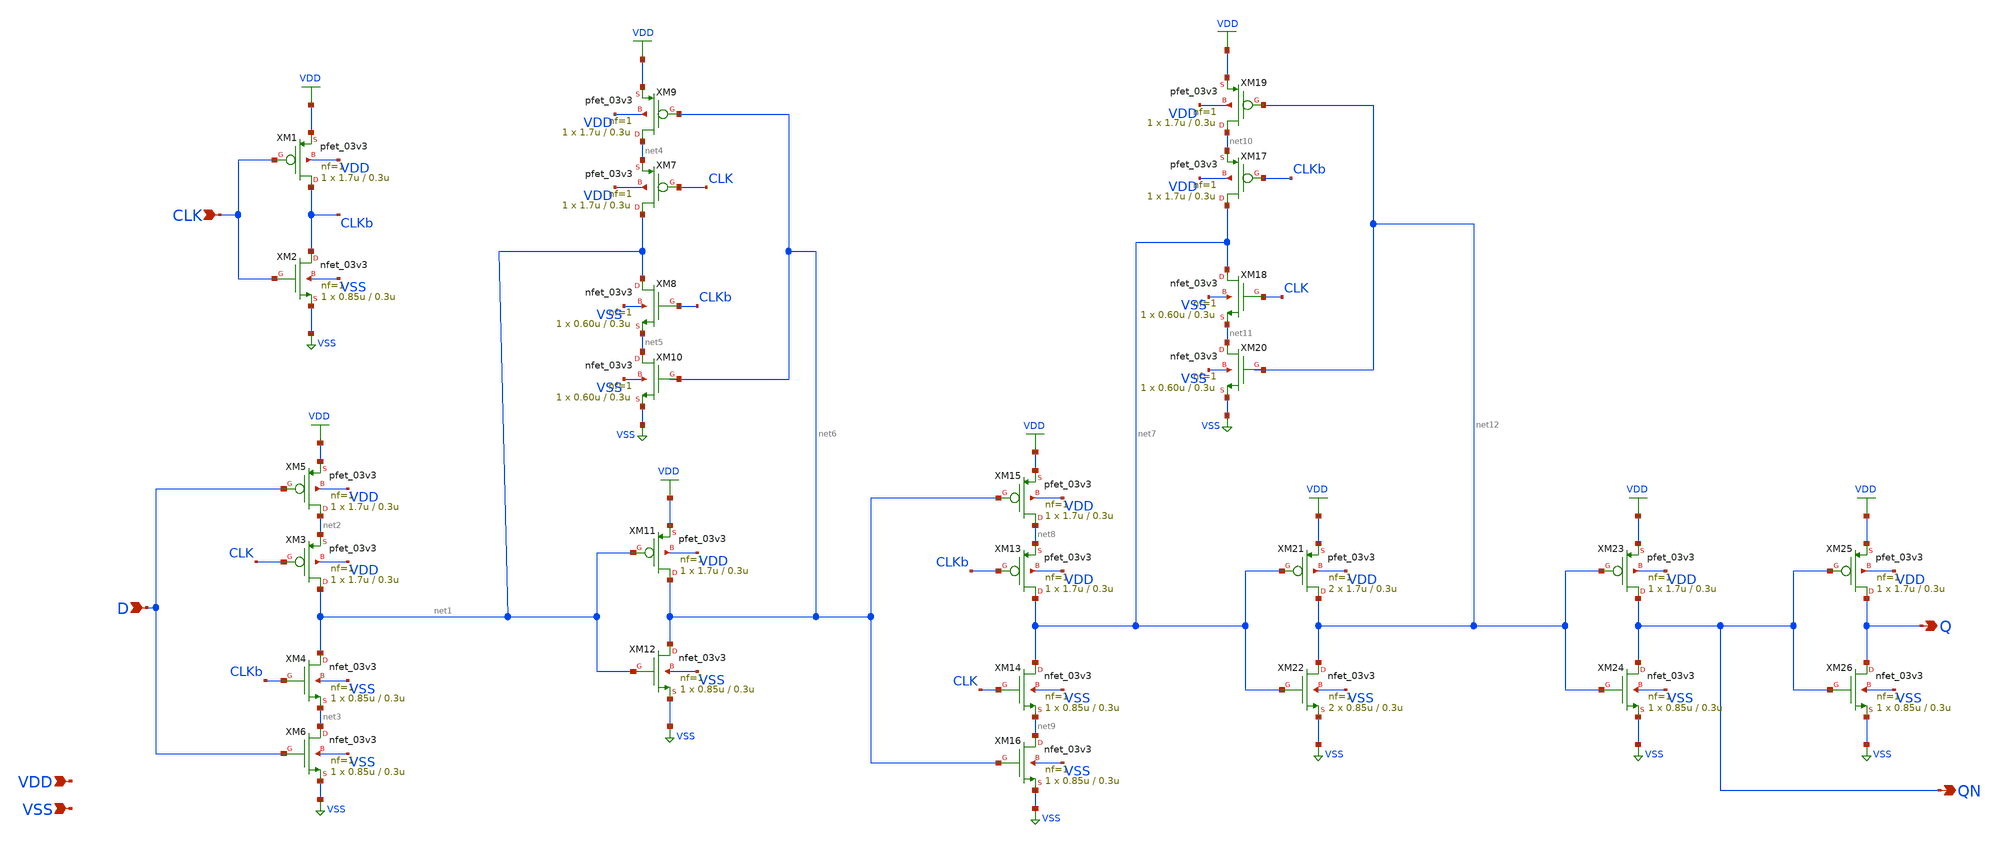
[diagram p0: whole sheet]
** sch_path: gf180mcu_osu_sc_gp9t3v3/xschem/gf180mcu_osu_sc_gp9t3v3__dff_1.sch
**.subckt gf180mcu_osu_sc_gp9t3v3__dff_1 D CLK Q QN VDD VSS
*.ipin D
*.ipin CLK
*.opin Q
*.opin QN
*.ipin VDD
*.ipin VSS
XM1 CLKb CLK VDD VDD pfet_03v3 L=0.3u W=1.7u nf=1 ad='int((nf+1)/2) * W/nf * 0.18u' as='int((nf+2)/2) * W/nf * 0.18u'
+ pd='2*int((nf+1)/2) * (W/nf + 0.18u)' ps='2*int((nf+2)/2) * (W/nf + 0.18u)' nrd='0.18u / W' nrs='0.18u / W'
+ sa=0 sb=0 sd=0 m=1
XM2 CLKb CLK VSS VSS nfet_03v3 L=0.3u W=0.85u nf=1 ad='int((nf+1)/2) * W/nf * 0.18u' as='int((nf+2)/2) * W/nf * 0.18u'
+ pd='2*int((nf+1)/2) * (W/nf + 0.18u)' ps='2*int((nf+2)/2) * (W/nf + 0.18u)' nrd='0.18u / W' nrs='0.18u / W'
+ sa=0 sb=0 sd=0 m=1
XM3 net1 CLK net2 VDD pfet_03v3 L=0.3u W=1.7u nf=1 ad='int((nf+1)/2) * W/nf * 0.18u' as='int((nf+2)/2) * W/nf * 0.18u'
+ pd='2*int((nf+1)/2) * (W/nf + 0.18u)' ps='2*int((nf+2)/2) * (W/nf + 0.18u)' nrd='0.18u / W' nrs='0.18u / W'
+ sa=0 sb=0 sd=0 m=1
XM4 net1 CLKb net3 VSS nfet_03v3 L=0.3u W=0.85u nf=1 ad='int((nf+1)/2) * W/nf * 0.18u' as='int((nf+2)/2) * W/nf * 0.18u'
+ pd='2*int((nf+1)/2) * (W/nf + 0.18u)' ps='2*int((nf+2)/2) * (W/nf + 0.18u)' nrd='0.18u / W' nrs='0.18u / W'
+ sa=0 sb=0 sd=0 m=1
XM5 net2 D VDD VDD pfet_03v3 L=0.3u W=1.7u nf=1 ad='int((nf+1)/2) * W/nf * 0.18u' as='int((nf+2)/2) * W/nf * 0.18u'
+ pd='2*int((nf+1)/2) * (W/nf + 0.18u)' ps='2*int((nf+2)/2) * (W/nf + 0.18u)' nrd='0.18u / W' nrs='0.18u / W'
+ sa=0 sb=0 sd=0 m=1
XM6 net3 D VSS VSS nfet_03v3 L=0.3u W=0.85u nf=1 ad='int((nf+1)/2) * W/nf * 0.18u' as='int((nf+2)/2) * W/nf * 0.18u'
+ pd='2*int((nf+1)/2) * (W/nf + 0.18u)' ps='2*int((nf+2)/2) * (W/nf + 0.18u)' nrd='0.18u / W' nrs='0.18u / W'
+ sa=0 sb=0 sd=0 m=1
XM7 net1 CLK net4 VDD pfet_03v3 L=0.3u W=1.7u nf=1 ad='int((nf+1)/2) * W/nf * 0.18u' as='int((nf+2)/2) * W/nf * 0.18u'
+ pd='2*int((nf+1)/2) * (W/nf + 0.18u)' ps='2*int((nf+2)/2) * (W/nf + 0.18u)' nrd='0.18u / W' nrs='0.18u / W'
+ sa=0 sb=0 sd=0 m=1
XM8 net1 CLKb net5 VSS nfet_03v3 L=0.3u W=0.60u nf=1 ad='int((nf+1)/2) * W/nf * 0.18u' as='int((nf+2)/2) * W/nf * 0.18u'
+ pd='2*int((nf+1)/2) * (W/nf + 0.18u)' ps='2*int((nf+2)/2) * (W/nf + 0.18u)' nrd='0.18u / W' nrs='0.18u / W'
+ sa=0 sb=0 sd=0 m=1
XM9 net4 net6 VDD VDD pfet_03v3 L=0.3u W=1.7u nf=1 ad='int((nf+1)/2) * W/nf * 0.18u' as='int((nf+2)/2) * W/nf * 0.18u'
+ pd='2*int((nf+1)/2) * (W/nf + 0.18u)' ps='2*int((nf+2)/2) * (W/nf + 0.18u)' nrd='0.18u / W' nrs='0.18u / W'
+ sa=0 sb=0 sd=0 m=1
XM10 net5 net6 VSS VSS nfet_03v3 L=0.3u W=0.60u nf=1 ad='int((nf+1)/2) * W/nf * 0.18u' as='int((nf+2)/2) * W/nf * 0.18u'
+ pd='2*int((nf+1)/2) * (W/nf + 0.18u)' ps='2*int((nf+2)/2) * (W/nf + 0.18u)' nrd='0.18u / W' nrs='0.18u / W'
+ sa=0 sb=0 sd=0 m=1
XM11 net6 net1 VDD VDD pfet_03v3 L=0.3u W=1.7u nf=1 ad='int((nf+1)/2) * W/nf * 0.18u' as='int((nf+2)/2) * W/nf * 0.18u'
+ pd='2*int((nf+1)/2) * (W/nf + 0.18u)' ps='2*int((nf+2)/2) * (W/nf + 0.18u)' nrd='0.18u / W' nrs='0.18u / W'
+ sa=0 sb=0 sd=0 m=1
XM12 net6 net1 VSS VSS nfet_03v3 L=0.3u W=0.85u nf=1 ad='int((nf+1)/2) * W/nf * 0.18u' as='int((nf+2)/2) * W/nf * 0.18u'
+ pd='2*int((nf+1)/2) * (W/nf + 0.18u)' ps='2*int((nf+2)/2) * (W/nf + 0.18u)' nrd='0.18u / W' nrs='0.18u / W'
+ sa=0 sb=0 sd=0 m=1
XM13 net7 CLKb net8 VDD pfet_03v3 L=0.3u W=1.7u nf=1 ad='int((nf+1)/2) * W/nf * 0.18u' as='int((nf+2)/2) * W/nf * 0.18u'
+ pd='2*int((nf+1)/2) * (W/nf + 0.18u)' ps='2*int((nf+2)/2) * (W/nf + 0.18u)' nrd='0.18u / W' nrs='0.18u / W'
+ sa=0 sb=0 sd=0 m=1
XM14 net7 CLK net9 VSS nfet_03v3 L=0.3u W=0.85u nf=1 ad='int((nf+1)/2) * W/nf * 0.18u' as='int((nf+2)/2) * W/nf * 0.18u'
+ pd='2*int((nf+1)/2) * (W/nf + 0.18u)' ps='2*int((nf+2)/2) * (W/nf + 0.18u)' nrd='0.18u / W' nrs='0.18u / W'
+ sa=0 sb=0 sd=0 m=1
XM15 net8 net6 VDD VDD pfet_03v3 L=0.3u W=1.7u nf=1 ad='int((nf+1)/2) * W/nf * 0.18u' as='int((nf+2)/2) * W/nf * 0.18u'
+ pd='2*int((nf+1)/2) * (W/nf + 0.18u)' ps='2*int((nf+2)/2) * (W/nf + 0.18u)' nrd='0.18u / W' nrs='0.18u / W'
+ sa=0 sb=0 sd=0 m=1
XM16 net9 net6 VSS VSS nfet_03v3 L=0.3u W=0.85u nf=1 ad='int((nf+1)/2) * W/nf * 0.18u' as='int((nf+2)/2) * W/nf * 0.18u'
+ pd='2*int((nf+1)/2) * (W/nf + 0.18u)' ps='2*int((nf+2)/2) * (W/nf + 0.18u)' nrd='0.18u / W' nrs='0.18u / W'
+ sa=0 sb=0 sd=0 m=1
XM17 net7 CLKb net10 VDD pfet_03v3 L=0.3u W=1.7u nf=1 ad='int((nf+1)/2) * W/nf * 0.18u' as='int((nf+2)/2) * W/nf * 0.18u'
+ pd='2*int((nf+1)/2) * (W/nf + 0.18u)' ps='2*int((nf+2)/2) * (W/nf + 0.18u)' nrd='0.18u / W' nrs='0.18u / W'
+ sa=0 sb=0 sd=0 m=1
XM18 net7 CLK net11 VSS nfet_03v3 L=0.3u W=0.60u nf=1 ad='int((nf+1)/2) * W/nf * 0.18u' as='int((nf+2)/2) * W/nf * 0.18u'
+ pd='2*int((nf+1)/2) * (W/nf + 0.18u)' ps='2*int((nf+2)/2) * (W/nf + 0.18u)' nrd='0.18u / W' nrs='0.18u / W'
+ sa=0 sb=0 sd=0 m=1
XM19 net10 net12 VDD VDD pfet_03v3 L=0.3u W=1.7u nf=1 ad='int((nf+1)/2) * W/nf * 0.18u' as='int((nf+2)/2) * W/nf * 0.18u'
+ pd='2*int((nf+1)/2) * (W/nf + 0.18u)' ps='2*int((nf+2)/2) * (W/nf + 0.18u)' nrd='0.18u / W' nrs='0.18u / W'
+ sa=0 sb=0 sd=0 m=1
XM20 net11 net12 VSS VSS nfet_03v3 L=0.3u W=0.60u nf=1 ad='int((nf+1)/2) * W/nf * 0.18u' as='int((nf+2)/2) * W/nf * 0.18u'
+ pd='2*int((nf+1)/2) * (W/nf + 0.18u)' ps='2*int((nf+2)/2) * (W/nf + 0.18u)' nrd='0.18u / W' nrs='0.18u / W'
+ sa=0 sb=0 sd=0 m=1
XM21 net12 net7 VDD VDD pfet_03v3 L=0.3u W=1.7u nf=1 ad='int((nf+1)/2) * W/nf * 0.18u' as='int((nf+2)/2) * W/nf * 0.18u'
+ pd='2*int((nf+1)/2) * (W/nf + 0.18u)' ps='2*int((nf+2)/2) * (W/nf + 0.18u)' nrd='0.18u / W' nrs='0.18u / W'
+ sa=0 sb=0 sd=0 m=2
XM22 net12 net7 VSS VSS nfet_03v3 L=0.3u W=0.85u nf=1 ad='int((nf+1)/2) * W/nf * 0.18u' as='int((nf+2)/2) * W/nf * 0.18u'
+ pd='2*int((nf+1)/2) * (W/nf + 0.18u)' ps='2*int((nf+2)/2) * (W/nf + 0.18u)' nrd='0.18u / W' nrs='0.18u / W'
+ sa=0 sb=0 sd=0 m=2
XM23 QN net12 VDD VDD pfet_03v3 L=0.3u W=1.7u nf=1 ad='int((nf+1)/2) * W/nf * 0.18u' as='int((nf+2)/2) * W/nf * 0.18u'
+ pd='2*int((nf+1)/2) * (W/nf + 0.18u)' ps='2*int((nf+2)/2) * (W/nf + 0.18u)' nrd='0.18u / W' nrs='0.18u / W'
+ sa=0 sb=0 sd=0 m=1
XM24 QN net12 VSS VSS nfet_03v3 L=0.3u W=0.85u nf=1 ad='int((nf+1)/2) * W/nf * 0.18u' as='int((nf+2)/2) * W/nf * 0.18u'
+ pd='2*int((nf+1)/2) * (W/nf + 0.18u)' ps='2*int((nf+2)/2) * (W/nf + 0.18u)' nrd='0.18u / W' nrs='0.18u / W'
+ sa=0 sb=0 sd=0 m=1
XM25 Q QN VDD VDD pfet_03v3 L=0.3u W=1.7u nf=1 ad='int((nf+1)/2) * W/nf * 0.18u' as='int((nf+2)/2) * W/nf * 0.18u'
+ pd='2*int((nf+1)/2) * (W/nf + 0.18u)' ps='2*int((nf+2)/2) * (W/nf + 0.18u)' nrd='0.18u / W' nrs='0.18u / W'
+ sa=0 sb=0 sd=0 m=1
XM26 Q QN VSS VSS nfet_03v3 L=0.3u W=0.85u nf=1 ad='int((nf+1)/2) * W/nf * 0.18u' as='int((nf+2)/2) * W/nf * 0.18u'
+ pd='2*int((nf+1)/2) * (W/nf + 0.18u)' ps='2*int((nf+2)/2) * (W/nf + 0.18u)' nrd='0.18u / W' nrs='0.18u / W'
+ sa=0 sb=0 sd=0 m=1
**.ends
.GLOBAL VDD
.GLOBAL VSS
.end
